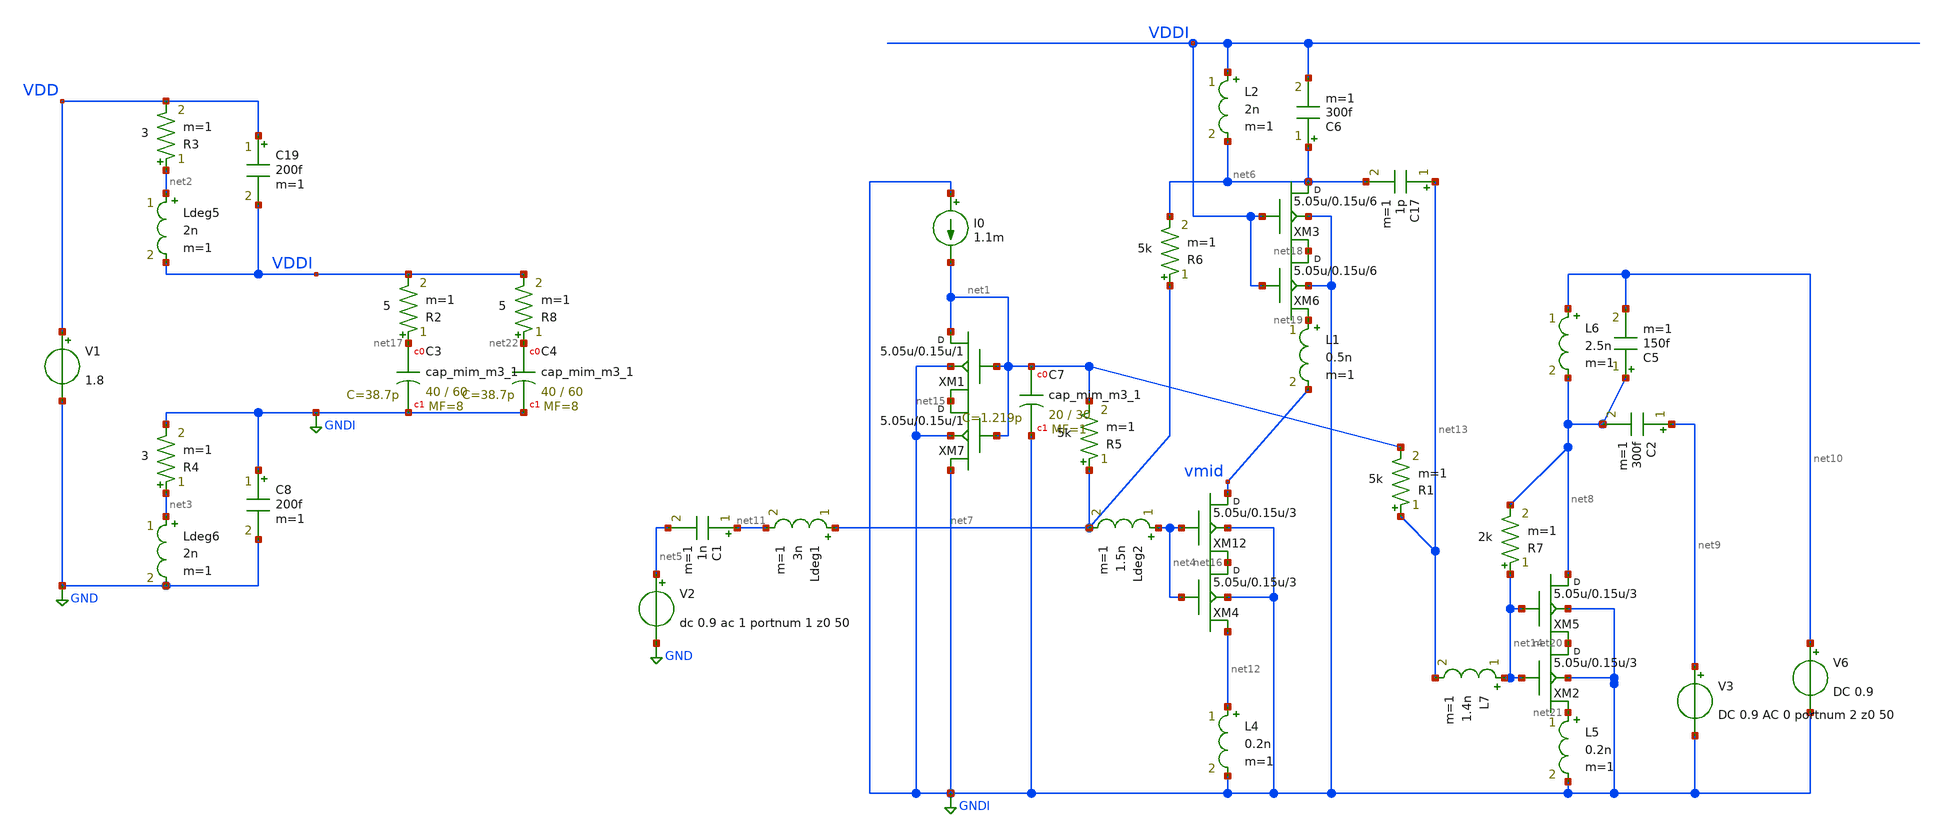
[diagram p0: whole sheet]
** sch_path: xschem/LNA5_with_output_buf_1.sch
**.subckt LNA5_with_output_buf_1
V1 VDD GND 1.8
V2 net5 GND dc 0.9 ac 1 portnum 1 z0 50
I0 GNDI net1 1.1m
XM1 net1 net1 net15 GNDI sky130_fd_pr__rf_nfet_01v8_bM04W5p00L0p15_ext w=5.05u l=0.15u m=1
XC7 net1 GNDI sky130_fd_pr__cap_mim_m3_1 W=20 L=30 MF=1 m=1
Ldeg5 net2 VDDI 2n m=1
R3 net2 VDD 3 m=1
Ldeg6 net3 GND 2n m=1
R4 net3 GNDI 3 m=1
XM12 vmid net4 net16 GNDI sky130_fd_pr__rf_nfet_01v8_bM04W5p00L0p15_ext w=5.05u l=0.15u m=3
C17 net13 net6 1p m=1
L2 VDDI net6 2n m=1
XC3 net17 GNDI sky130_fd_pr__cap_mim_m3_1 W=40 L=60 MF=8 m=8
C8 GNDI GND 200f m=1
C19 VDD VDDI 200f m=1
R2 net17 VDDI 5 m=1
R5 net7 net1 5k m=1
XM4 net16 net4 net12 GNDI sky130_fd_pr__rf_nfet_01v8_bM04W5p00L0p15_ext w=5.05u l=0.15u m=3
C1 net11 net5 1n m=1
C6 net6 VDDI 300f m=1
R6 net7 net6 5k m=1
XM3 net6 VDDI net18 GNDI sky130_fd_pr__rf_nfet_01v8_bM04W5p00L0p15_ext w=5.05u l=0.15u m=6
XM6 net18 VDDI net19 GNDI sky130_fd_pr__rf_nfet_01v8_bM04W5p00L0p15_ext w=5.05u l=0.15u m=6
XM7 net15 net1 GNDI GNDI sky130_fd_pr__rf_nfet_01v8_bM04W5p00L0p15_ext w=5.05u l=0.15u m=1
Ldeg1 net7 net11 3n m=1
L1 net19 vmid 0.5n m=1
L4 net12 GNDI 0.2n m=1
Ldeg2 net4 net7 1.5n m=1
XM2 net20 net14 net21 GNDI sky130_fd_pr__rf_nfet_01v8_bM04W5p00L0p15_ext w=5.05u l=0.15u m=3
V3 net9 GNDI DC 0.9 AC 0 portnum 2 z0 50
L5 net21 GNDI 0.2n m=1
C2 net9 net8 300f m=1
L6 net10 net8 2.5n m=1
V6 net10 GNDI DC 0.9
L7 net14 net13 1.4n m=1
R1 net13 net1 5k m=1
XM5 net8 net14 net20 GNDI sky130_fd_pr__rf_nfet_01v8_bM04W5p00L0p15_ext w=5.05u l=0.15u m=3
R7 net14 net8 2k m=1
XC4 net22 GNDI sky130_fd_pr__cap_mim_m3_1 W=40 L=60 MF=8 m=8
R8 net22 VDDI 5 m=1
C5 net8 net10 150f m=1
**** begin user architecture code
.lib $::SKYWATER_MODELS/sky130.lib.spice tt
* .include $::PDKPATH/libs.ref/sky130_fd_sc_hvl/spice/sky130_fd_sc_hvl.spice



.subckt sky130_fd_pr__rf_nfet_01v8_bM04W5p00L0p15_ext DRAIN GATE SOURCE SUBSTRATE
X0 DRAIN GATE SOURCE SUBSTRATE sky130_fd_pr__nfet_01v8 ad=2.828e+12p pd=2.132e+07u as=4.242e+12p
+ ps=3.198e+07u w=5.05e+06u l=150000u
X1 SOURCE SUBSTRATE SUBSTRATE SUBSTRATE sky130_fd_pr__nfet_01v8 ad=0p pd=0u as=3.03e+12p
+ ps=2.14e+07u w=5.05e+06u l=150000u
X2 SOURCE GATE DRAIN SUBSTRATE sky130_fd_pr__nfet_01v8 ad=0p pd=0u as=0p ps=0u w=5.05e+06u l=150000u
X3 DRAIN GATE SOURCE SUBSTRATE sky130_fd_pr__nfet_01v8 ad=0p pd=0u as=0p ps=0u w=5.05e+06u l=150000u
X4 SUBSTRATE SUBSTRATE SOURCE SUBSTRATE sky130_fd_pr__nfet_01v8 ad=0p pd=0u as=0p ps=0u w=5.05e+06u
+ l=150000u
X5 SOURCE GATE DRAIN SUBSTRATE sky130_fd_pr__nfet_01v8 ad=0p pd=0u as=0p ps=0u w=5.05e+06u l=150000u
.ends
.sp dec 1000 1e9 10e9 1
* .ac dec 1000 0.01e9 100e9
.control
run
display
let z11=50*(1+s_1_1)/(1-s_1_1)
let z22=50*(1+s_2_2)/(1-s_2_2)
let S11 = S_1_1
let S21 = S_2_1
let S12 = S_1_2
let S22 = S_2_2

* Stability
let delta=S11*S22-S12*S21
let K    = (1-mag(S11)^2-mag(S22)^2+mag(delta)^2)/(2*mag(S12*S21))
let mu   = (1-mag(S11)^2)/(mag(S22-conj(S11)*delta)+mag(S21*S12))
* plot real(z11) real(z22)
* plot imag(z11) imag(z22)
plot db(S_1_1) db(S_2_2) db(S_2_1)

plot db(K)
plot mag(delta)
plot db(mu)
plot NF NFmin
.endc


**** end user architecture code
**.ends
.GLOBAL GND
.GLOBAL GNDI
.end
